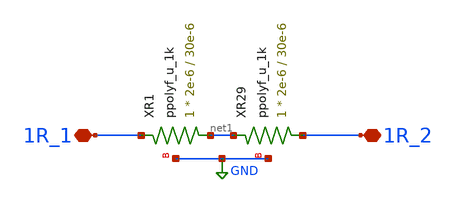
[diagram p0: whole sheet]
** sch_path: xschem/1R.sch
**.subckt 1R 1R_1 1R_2
*.iopin 1R_1
*.iopin 1R_2
XR1 net1 1R_1 GND ppolyf_u_1k r_width=2e-6 r_length=30e-6 m=1
XR29 1R_2 net1 GND ppolyf_u_1k r_width=2e-6 r_length=30e-6 m=1
**.ends
.GLOBAL GND
.end
